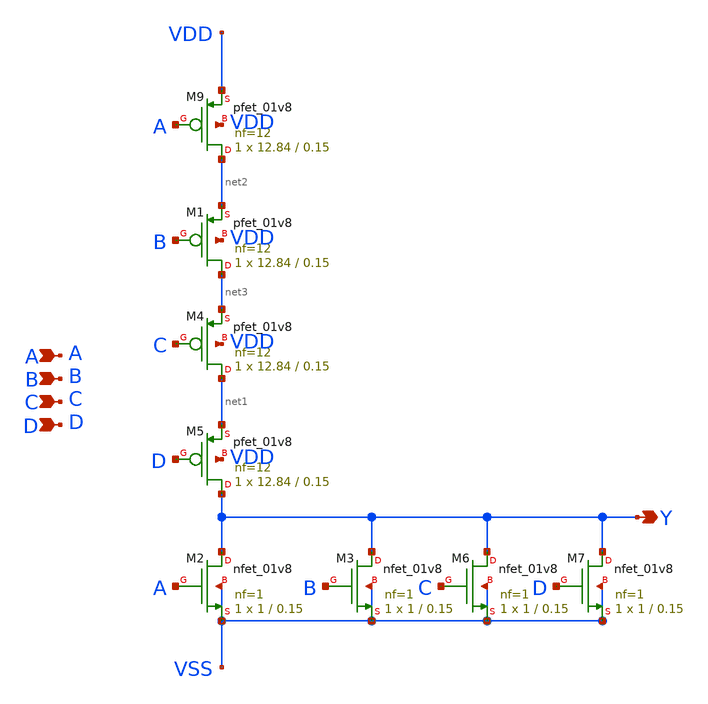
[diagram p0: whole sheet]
** sch_path: design/xschem/NOR/nor4.sch
**.subckt nor4 Y B D C A
*.opin Y
*.ipin B
*.ipin D
*.ipin C
*.ipin A
XM2 Y A VSS VSS sky130_fd_pr__nfet_01v8 L=0.15 W=1 nf=1 ad='int((nf+1)/2) * W/nf * 0.29' as='int((nf+2)/2) * W/nf * 0.29'
+ pd='2*int((nf+1)/2) * (W/nf + 0.29)' ps='2*int((nf+2)/2) * (W/nf + 0.29)' nrd='0.29 / W' nrs='0.29 / W'
+ sa=0 sb=0 sd=0 mult=1 m=1
XM3 Y B VSS VSS sky130_fd_pr__nfet_01v8 L=0.15 W=1 nf=1 ad='int((nf+1)/2) * W/nf * 0.29' as='int((nf+2)/2) * W/nf * 0.29'
+ pd='2*int((nf+1)/2) * (W/nf + 0.29)' ps='2*int((nf+2)/2) * (W/nf + 0.29)' nrd='0.29 / W' nrs='0.29 / W'
+ sa=0 sb=0 sd=0 mult=1 m=1
XM6 Y C VSS VSS sky130_fd_pr__nfet_01v8 L=0.15 W=1 nf=1 ad='int((nf+1)/2) * W/nf * 0.29' as='int((nf+2)/2) * W/nf * 0.29'
+ pd='2*int((nf+1)/2) * (W/nf + 0.29)' ps='2*int((nf+2)/2) * (W/nf + 0.29)' nrd='0.29 / W' nrs='0.29 / W'
+ sa=0 sb=0 sd=0 mult=1 m=1
XM7 Y D VSS VSS sky130_fd_pr__nfet_01v8 L=0.15 W=1 nf=1 ad='int((nf+1)/2) * W/nf * 0.29' as='int((nf+2)/2) * W/nf * 0.29'
+ pd='2*int((nf+1)/2) * (W/nf + 0.29)' ps='2*int((nf+2)/2) * (W/nf + 0.29)' nrd='0.29 / W' nrs='0.29 / W'
+ sa=0 sb=0 sd=0 mult=1 m=1
XM9 net2 A VDD VDD sky130_fd_pr__pfet_01v8 L=0.15 W=12.84 nf=12 ad='int((nf+1)/2) * W/nf * 0.29' as='int((nf+2)/2) * W/nf * 0.29'
+ pd='2*int((nf+1)/2) * (W/nf + 0.29)' ps='2*int((nf+2)/2) * (W/nf + 0.29)' nrd='0.29 / W' nrs='0.29 / W'
+ sa=0 sb=0 sd=0 mult=1 m=1
XM1 net3 B net2 VDD sky130_fd_pr__pfet_01v8 L=0.15 W=12.84 nf=12 ad='int((nf+1)/2) * W/nf * 0.29' as='int((nf+2)/2) * W/nf * 0.29'
+ pd='2*int((nf+1)/2) * (W/nf + 0.29)' ps='2*int((nf+2)/2) * (W/nf + 0.29)' nrd='0.29 / W' nrs='0.29 / W'
+ sa=0 sb=0 sd=0 mult=1 m=1
XM4 net1 C net3 VDD sky130_fd_pr__pfet_01v8 L=0.15 W=12.84 nf=12 ad='int((nf+1)/2) * W/nf * 0.29' as='int((nf+2)/2) * W/nf * 0.29'
+ pd='2*int((nf+1)/2) * (W/nf + 0.29)' ps='2*int((nf+2)/2) * (W/nf + 0.29)' nrd='0.29 / W' nrs='0.29 / W'
+ sa=0 sb=0 sd=0 mult=1 m=1
XM5 Y D net1 VDD sky130_fd_pr__pfet_01v8 L=0.15 W=12.84 nf=12 ad='int((nf+1)/2) * W/nf * 0.29' as='int((nf+2)/2) * W/nf * 0.29'
+ pd='2*int((nf+1)/2) * (W/nf + 0.29)' ps='2*int((nf+2)/2) * (W/nf + 0.29)' nrd='0.29 / W' nrs='0.29 / W'
+ sa=0 sb=0 sd=0 mult=1 m=1
**.ends
.end
